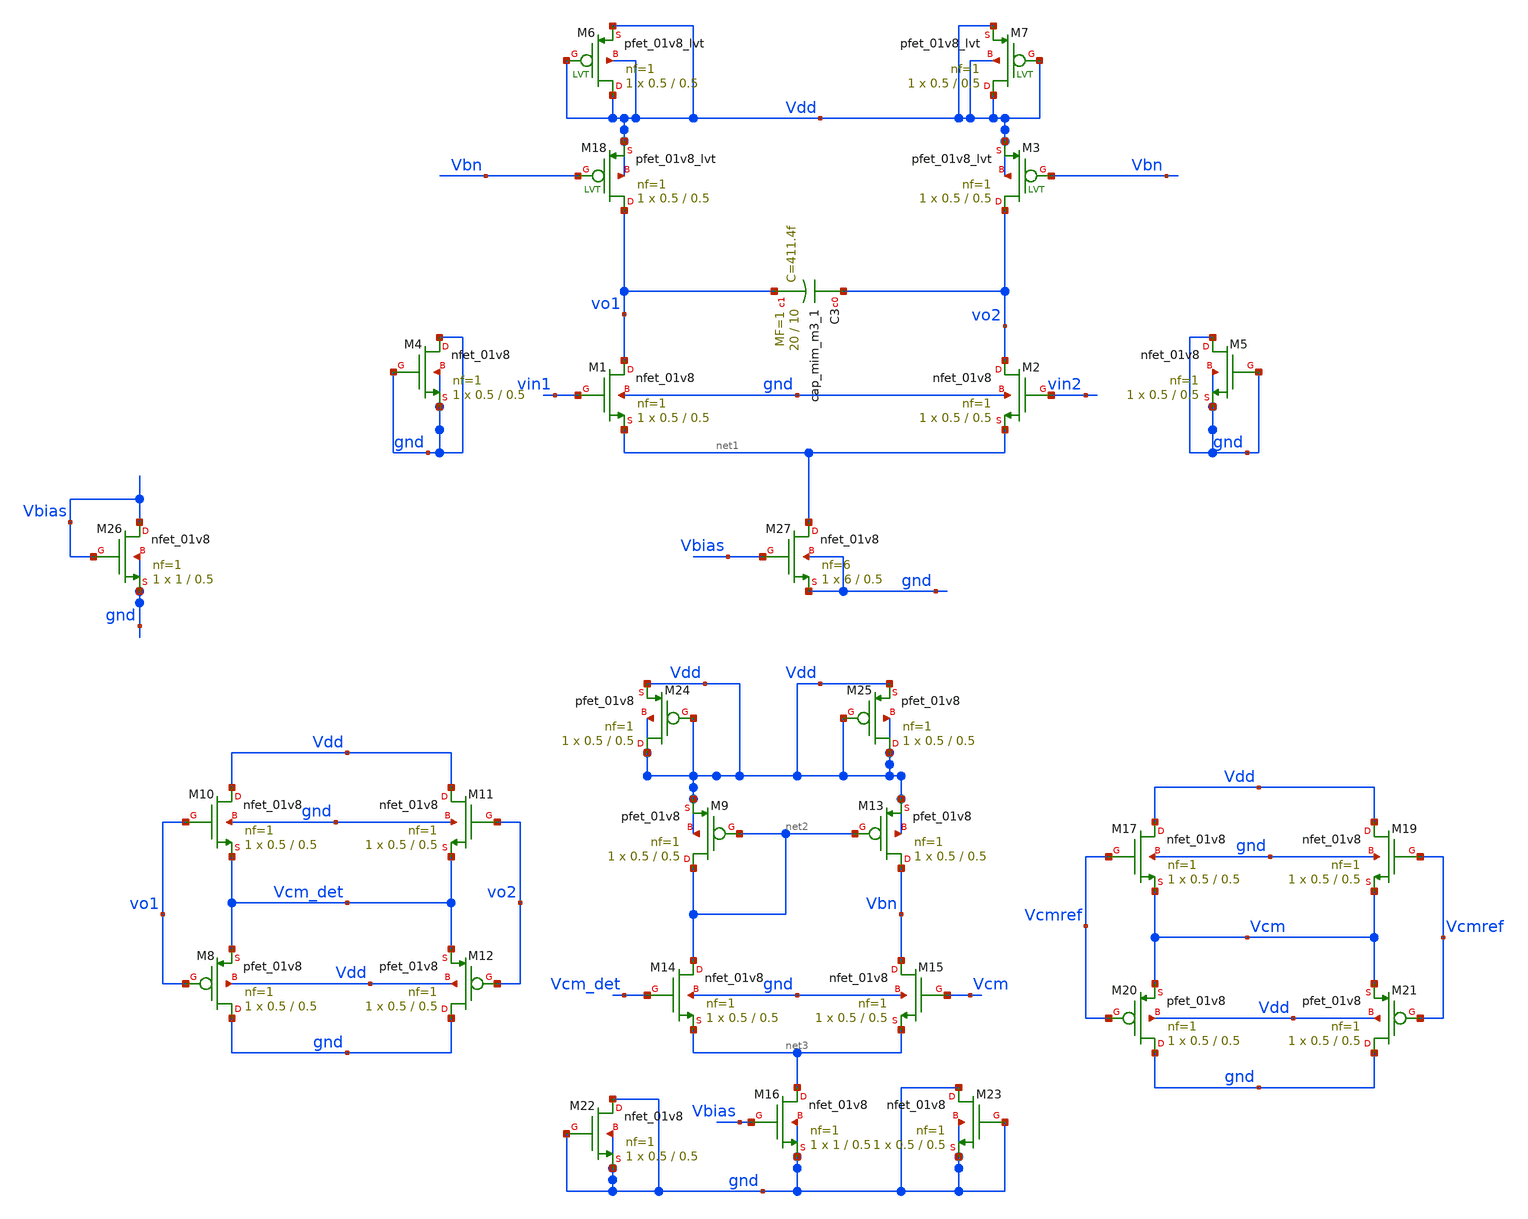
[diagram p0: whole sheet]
** sch_path: xschem/xschemfiles/integrator_full_new1.sch
**.subckt integrator_full_new1
XM1 vo1 vin1 net1 gnd sky130_fd_pr__nfet_01v8 L=0.5 W=0.5 nf=1 ad='int((nf+1)/2) * W/nf * 0.29' as='int((nf+2)/2) * W/nf * 0.29'
+ pd='2*int((nf+1)/2) * (W/nf + 0.29)' ps='2*int((nf+2)/2) * (W/nf + 0.29)' nrd='0.29 / W' nrs='0.29 / W'
+ sa=0 sb=0 sd=0 mult=1 m=1
XM2 vo2 vin2 net1 gnd sky130_fd_pr__nfet_01v8 L=0.5 W=0.5 nf=1 ad='int((nf+1)/2) * W/nf * 0.29' as='int((nf+2)/2) * W/nf * 0.29'
+ pd='2*int((nf+1)/2) * (W/nf + 0.29)' ps='2*int((nf+2)/2) * (W/nf + 0.29)' nrd='0.29 / W' nrs='0.29 / W'
+ sa=0 sb=0 sd=0 mult=1 m=1
XC3 vo2 vo1 sky130_fd_pr__cap_mim_m3_1 W=20 L=10 MF=1 m=1
XM4 gnd gnd gnd gnd sky130_fd_pr__nfet_01v8 L=0.5 W=0.5 nf=1 ad='int((nf+1)/2) * W/nf * 0.29' as='int((nf+2)/2) * W/nf * 0.29'
+ pd='2*int((nf+1)/2) * (W/nf + 0.29)' ps='2*int((nf+2)/2) * (W/nf + 0.29)' nrd='0.29 / W' nrs='0.29 / W'
+ sa=0 sb=0 sd=0 mult=1 m=1
XM5 gnd gnd gnd gnd sky130_fd_pr__nfet_01v8 L=0.5 W=0.5 nf=1 ad='int((nf+1)/2) * W/nf * 0.29' as='int((nf+2)/2) * W/nf * 0.29'
+ pd='2*int((nf+1)/2) * (W/nf + 0.29)' ps='2*int((nf+2)/2) * (W/nf + 0.29)' nrd='0.29 / W' nrs='0.29 / W'
+ sa=0 sb=0 sd=0 mult=1 m=1
XM8 gnd vo1 Vcm_det Vdd sky130_fd_pr__pfet_01v8 L=0.5 W=0.5 nf=1 ad='int((nf+1)/2) * W/nf * 0.29' as='int((nf+2)/2) * W/nf * 0.29'
+ pd='2*int((nf+1)/2) * (W/nf + 0.29)' ps='2*int((nf+2)/2) * (W/nf + 0.29)' nrd='0.29 / W' nrs='0.29 / W'
+ sa=0 sb=0 sd=0 mult=1 m=1
XM12 gnd vo2 Vcm_det Vdd sky130_fd_pr__pfet_01v8 L=0.5 W=0.5 nf=1 ad='int((nf+1)/2) * W/nf * 0.29' as='int((nf+2)/2) * W/nf * 0.29'
+ pd='2*int((nf+1)/2) * (W/nf + 0.29)' ps='2*int((nf+2)/2) * (W/nf + 0.29)' nrd='0.29 / W' nrs='0.29 / W'
+ sa=0 sb=0 sd=0 mult=1 m=1
XM10 Vdd vo1 Vcm_det gnd sky130_fd_pr__nfet_01v8 L=0.5 W=0.5 nf=1 ad='int((nf+1)/2) * W/nf * 0.29' as='int((nf+2)/2) * W/nf * 0.29'
+ pd='2*int((nf+1)/2) * (W/nf + 0.29)' ps='2*int((nf+2)/2) * (W/nf + 0.29)' nrd='0.29 / W' nrs='0.29 / W'
+ sa=0 sb=0 sd=0 mult=1 m=1
XM11 Vdd vo2 Vcm_det gnd sky130_fd_pr__nfet_01v8 L=0.5 W=0.5 nf=1 ad='int((nf+1)/2) * W/nf * 0.29' as='int((nf+2)/2) * W/nf * 0.29'
+ pd='2*int((nf+1)/2) * (W/nf + 0.29)' ps='2*int((nf+2)/2) * (W/nf + 0.29)' nrd='0.29 / W' nrs='0.29 / W'
+ sa=0 sb=0 sd=0 mult=1 m=1
XM9 net2 net2 Vdd Vdd sky130_fd_pr__pfet_01v8 L=0.5 W=0.5 nf=1 ad='int((nf+1)/2) * W/nf * 0.29' as='int((nf+2)/2) * W/nf * 0.29'
+ pd='2*int((nf+1)/2) * (W/nf + 0.29)' ps='2*int((nf+2)/2) * (W/nf + 0.29)' nrd='0.29 / W' nrs='0.29 / W'
+ sa=0 sb=0 sd=0 mult=1 m=1
XM13 Vbn net2 Vdd Vdd sky130_fd_pr__pfet_01v8 L=0.5 W=0.5 nf=1 ad='int((nf+1)/2) * W/nf * 0.29' as='int((nf+2)/2) * W/nf * 0.29'
+ pd='2*int((nf+1)/2) * (W/nf + 0.29)' ps='2*int((nf+2)/2) * (W/nf + 0.29)' nrd='0.29 / W' nrs='0.29 / W'
+ sa=0 sb=0 sd=0 mult=1 m=1
XM14 net2 Vcm_det net3 gnd sky130_fd_pr__nfet_01v8 L=0.5 W=0.5 nf=1 ad='int((nf+1)/2) * W/nf * 0.29'
+ as='int((nf+2)/2) * W/nf * 0.29' pd='2*int((nf+1)/2) * (W/nf + 0.29)' ps='2*int((nf+2)/2) * (W/nf + 0.29)'
+ nrd='0.29 / W' nrs='0.29 / W' sa=0 sb=0 sd=0 mult=1 m=1
XM15 Vbn Vcm net3 gnd sky130_fd_pr__nfet_01v8 L=0.5 W=0.5 nf=1 ad='int((nf+1)/2) * W/nf * 0.29' as='int((nf+2)/2) * W/nf * 0.29'
+ pd='2*int((nf+1)/2) * (W/nf + 0.29)' ps='2*int((nf+2)/2) * (W/nf + 0.29)' nrd='0.29 / W' nrs='0.29 / W'
+ sa=0 sb=0 sd=0 mult=1 m=1
XM16 net3 Vbias gnd gnd sky130_fd_pr__nfet_01v8 L=0.5 W=1 nf=1 ad='int((nf+1)/2) * W/nf * 0.29' as='int((nf+2)/2) * W/nf * 0.29'
+ pd='2*int((nf+1)/2) * (W/nf + 0.29)' ps='2*int((nf+2)/2) * (W/nf + 0.29)' nrd='0.29 / W' nrs='0.29 / W'
+ sa=0 sb=0 sd=0 mult=1 m=1
XM17 Vdd Vcmref Vcm gnd sky130_fd_pr__nfet_01v8 L=0.5 W=0.5 nf=1 ad='int((nf+1)/2) * W/nf * 0.29' as='int((nf+2)/2) * W/nf * 0.29'
+ pd='2*int((nf+1)/2) * (W/nf + 0.29)' ps='2*int((nf+2)/2) * (W/nf + 0.29)' nrd='0.29 / W' nrs='0.29 / W'
+ sa=0 sb=0 sd=0 mult=1 m=1
XM19 Vdd Vcmref Vcm gnd sky130_fd_pr__nfet_01v8 L=0.5 W=0.5 nf=1 ad='int((nf+1)/2) * W/nf * 0.29' as='int((nf+2)/2) * W/nf * 0.29'
+ pd='2*int((nf+1)/2) * (W/nf + 0.29)' ps='2*int((nf+2)/2) * (W/nf + 0.29)' nrd='0.29 / W' nrs='0.29 / W'
+ sa=0 sb=0 sd=0 mult=1 m=1
XM20 gnd Vcmref Vcm Vdd sky130_fd_pr__pfet_01v8 L=0.5 W=0.5 nf=1 ad='int((nf+1)/2) * W/nf * 0.29' as='int((nf+2)/2) * W/nf * 0.29'
+ pd='2*int((nf+1)/2) * (W/nf + 0.29)' ps='2*int((nf+2)/2) * (W/nf + 0.29)' nrd='0.29 / W' nrs='0.29 / W'
+ sa=0 sb=0 sd=0 mult=1 m=1
XM21 gnd Vcmref Vcm Vdd sky130_fd_pr__pfet_01v8 L=0.5 W=0.5 nf=1 ad='int((nf+1)/2) * W/nf * 0.29' as='int((nf+2)/2) * W/nf * 0.29'
+ pd='2*int((nf+1)/2) * (W/nf + 0.29)' ps='2*int((nf+2)/2) * (W/nf + 0.29)' nrd='0.29 / W' nrs='0.29 / W'
+ sa=0 sb=0 sd=0 mult=1 m=1
XM22 gnd gnd gnd gnd sky130_fd_pr__nfet_01v8 L=0.5 W=0.5 nf=1 ad='int((nf+1)/2) * W/nf * 0.29' as='int((nf+2)/2) * W/nf * 0.29'
+ pd='2*int((nf+1)/2) * (W/nf + 0.29)' ps='2*int((nf+2)/2) * (W/nf + 0.29)' nrd='0.29 / W' nrs='0.29 / W'
+ sa=0 sb=0 sd=0 mult=1 m=1
XM23 gnd gnd gnd gnd sky130_fd_pr__nfet_01v8 L=0.5 W=0.5 nf=1 ad='int((nf+1)/2) * W/nf * 0.29' as='int((nf+2)/2) * W/nf * 0.29'
+ pd='2*int((nf+1)/2) * (W/nf + 0.29)' ps='2*int((nf+2)/2) * (W/nf + 0.29)' nrd='0.29 / W' nrs='0.29 / W'
+ sa=0 sb=0 sd=0 mult=1 m=1
XM24 Vdd Vdd Vdd Vdd sky130_fd_pr__pfet_01v8 L=0.5 W=0.5 nf=1 ad='int((nf+1)/2) * W/nf * 0.29' as='int((nf+2)/2) * W/nf * 0.29'
+ pd='2*int((nf+1)/2) * (W/nf + 0.29)' ps='2*int((nf+2)/2) * (W/nf + 0.29)' nrd='0.29 / W' nrs='0.29 / W'
+ sa=0 sb=0 sd=0 mult=1 m=1
XM25 Vdd Vdd Vdd Vdd sky130_fd_pr__pfet_01v8 L=0.5 W=0.5 nf=1 ad='int((nf+1)/2) * W/nf * 0.29' as='int((nf+2)/2) * W/nf * 0.29'
+ pd='2*int((nf+1)/2) * (W/nf + 0.29)' ps='2*int((nf+2)/2) * (W/nf + 0.29)' nrd='0.29 / W' nrs='0.29 / W'
+ sa=0 sb=0 sd=0 mult=1 m=1
XM26 Vbias Vbias gnd gnd sky130_fd_pr__nfet_01v8 L=0.5 W=1 nf=1 ad='int((nf+1)/2) * W/nf * 0.29' as='int((nf+2)/2) * W/nf * 0.29'
+ pd='2*int((nf+1)/2) * (W/nf + 0.29)' ps='2*int((nf+2)/2) * (W/nf + 0.29)' nrd='0.29 / W' nrs='0.29 / W'
+ sa=0 sb=0 sd=0 mult=1 m=1
XM18 vo1 Vbn Vdd Vdd sky130_fd_pr__pfet_01v8_lvt L=0.5 W=0.5 nf=1 ad='int((nf+1)/2) * W/nf * 0.29' as='int((nf+2)/2) * W/nf * 0.29'
+ pd='2*int((nf+1)/2) * (W/nf + 0.29)' ps='2*int((nf+2)/2) * (W/nf + 0.29)' nrd='0.29 / W' nrs='0.29 / W'
+ sa=0 sb=0 sd=0 mult=1 m=1
XM6 Vdd Vdd Vdd Vdd sky130_fd_pr__pfet_01v8_lvt L=0.5 W=0.5 nf=1 ad='int((nf+1)/2) * W/nf * 0.29' as='int((nf+2)/2) * W/nf * 0.29'
+ pd='2*int((nf+1)/2) * (W/nf + 0.29)' ps='2*int((nf+2)/2) * (W/nf + 0.29)' nrd='0.29 / W' nrs='0.29 / W'
+ sa=0 sb=0 sd=0 mult=1 m=1
XM3 vo2 Vbn Vdd Vdd sky130_fd_pr__pfet_01v8_lvt L=0.5 W=0.5 nf=1 ad='int((nf+1)/2) * W/nf * 0.29' as='int((nf+2)/2) * W/nf * 0.29'
+ pd='2*int((nf+1)/2) * (W/nf + 0.29)' ps='2*int((nf+2)/2) * (W/nf + 0.29)' nrd='0.29 / W' nrs='0.29 / W'
+ sa=0 sb=0 sd=0 mult=1 m=1
XM7 Vdd Vdd Vdd Vdd sky130_fd_pr__pfet_01v8_lvt L=0.5 W=0.5 nf=1 ad='int((nf+1)/2) * W/nf * 0.29' as='int((nf+2)/2) * W/nf * 0.29'
+ pd='2*int((nf+1)/2) * (W/nf + 0.29)' ps='2*int((nf+2)/2) * (W/nf + 0.29)' nrd='0.29 / W' nrs='0.29 / W'
+ sa=0 sb=0 sd=0 mult=1 m=1
XM27 net1 Vbias gnd gnd sky130_fd_pr__nfet_01v8 L=0.5 W=6 nf=6 ad='int((nf+1)/2) * W/nf * 0.29' as='int((nf+2)/2) * W/nf * 0.29'
+ pd='2*int((nf+1)/2) * (W/nf + 0.29)' ps='2*int((nf+2)/2) * (W/nf + 0.29)' nrd='0.29 / W' nrs='0.29 / W'
+ sa=0 sb=0 sd=0 mult=1 m=1
**** begin user architecture code

** opencircuitdesign pdks install
.lib $::SKYWATER_MODELS/sky130.lib.spice tt


**** end user architecture code
**.ends
.end
